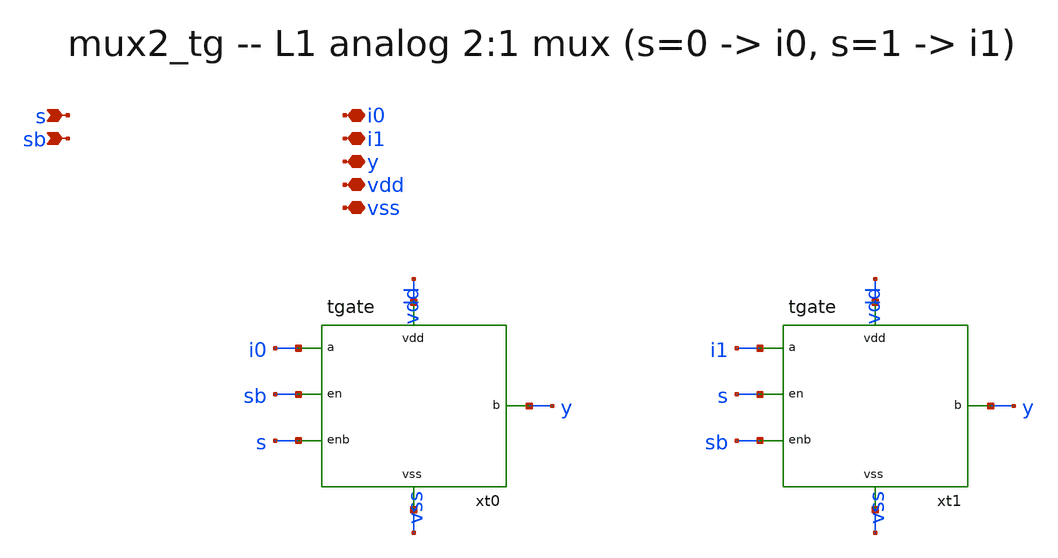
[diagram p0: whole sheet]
** sch_path: xschem/onetops/mux2_tg.sch
**.subckt mux2_tg s sb i0 i1 y vdd vss
*.ipin s
*.ipin sb
*.iopin i0
*.iopin i1
*.iopin y
*.iopin vdd
*.iopin vss
xt0 i0 sb s y vdd vss tgate
xt1 i1 s sb y vdd vss tgate
**.ends

* expanding   symbol:  onetops/tgate.sym # of pins=6
** sym_path: xschem/onetops/tgate.sym
** sch_path: xschem/onetops/tgate.sch
.subckt tgate a en enb b vdd vss
*.ipin en
*.ipin enb
*.iopin a
*.iopin b
*.iopin vdd
*.iopin vss
XMN1 a en b vss sky130_fd_pr__nfet_01v8 L=0.15 W=1 nf=1 ad='int((1 + 1)/2) * 1 / 1 * 0.29' as='int((1 + 2)/2) * 1 / 1 * 0.29'
+ pd='2*int((1 + 1)/2) * (1 / 1 + 0.29)' ps='2*int((1 + 2)/2) * (1 / 1 + 0.29)' nrd='0.29 / 1 ' nrs='0.29 / 1 '
+ sa=0 sb=0 sd=0 mult=1 m=1
XMP1 b enb a vdd sky130_fd_pr__pfet_01v8 L=0.15 W=2 nf=1 ad='int((1 + 1)/2) * 2 / 1 * 0.29' as='int((1 + 2)/2) * 2 / 1 * 0.29'
+ pd='2*int((1 + 1)/2) * (2 / 1 + 0.29)' ps='2*int((1 + 2)/2) * (2 / 1 + 0.29)' nrd='0.29 / 2 ' nrs='0.29 / 2 '
+ sa=0 sb=0 sd=0 mult=1 m=1
.ends

.end
